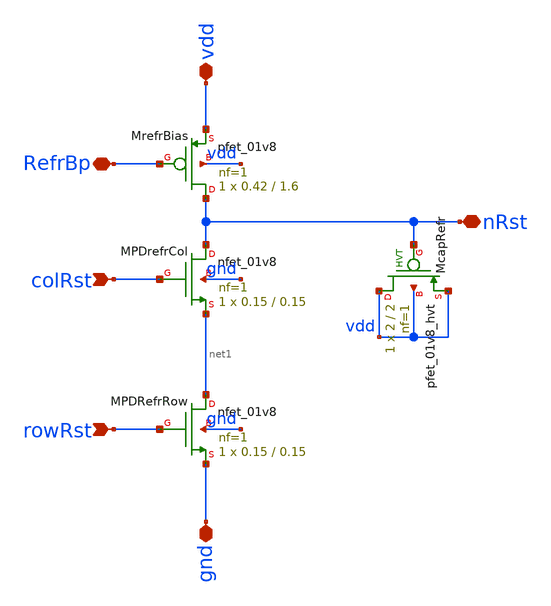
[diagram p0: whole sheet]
** sch_path: analog/xschem/PixelResetGen.sch
**.subckt PixelResetGen rowRst colRst RefrBp gnd vdd nRst
*.ipin rowRst
*.ipin colRst
*.iopin RefrBp
*.iopin gnd
*.iopin vdd
*.iopin nRst
XMPDrefrCol nRst colRst net1 gnd sky130_fd_pr__nfet_01v8 L=0.15 W=0.15 nf=1 ad='int((1 + 1)/2) * 0.15 / 1 * 0.29'
+ as='int((1 + 2)/2) * 0.15 / 1 * 0.29' pd='2*int((1 + 1)/2) * (0.15 / 1 + 0.29)' ps='2*int((1 + 2)/2) * (0.15 / 1 + 0.29)'
+ nrd='0.29 / 0.15 ' nrs='0.29 / 0.15 ' sa=0 sb=0 sd=0 mult=1 m=1
XMrefrBias nRst RefrBp vdd vdd sky130_fd_pr__pfet_01v8 L=1.6 W=0.42 nf=1 ad='int((1 + 1)/2) * 0.42 / 1 * 0.29'
+ as='int((1 + 2)/2) * 0.42 / 1 * 0.29' pd='2*int((1 + 1)/2) * (0.42 / 1 + 0.29)' ps='2*int((1 + 2)/2) * (0.42 / 1 + 0.29)'
+ nrd='0.29 / 0.42 ' nrs='0.29 / 0.42 ' sa=0 sb=0 sd=0 mult=1 m=1
XMcapRefr vdd nRst vdd vdd sky130_fd_pr__pfet_01v8_hvt L=2 W=2 nf=1 ad='int((1 + 1)/2) * 2 / 1 * 0.29'
+ as='int((1 + 2)/2) * 2 / 1 * 0.29' pd='2*int((1 + 1)/2) * (2 / 1 + 0.29)' ps='2*int((1 + 2)/2) * (2 / 1 + 0.29)'
+ nrd='0.29 / 2 ' nrs='0.29 / 2 ' sa=0 sb=0 sd=0 mult=1 m=1
XMPDRefrRow net1 rowRst gnd gnd sky130_fd_pr__nfet_01v8 L=0.15 W=0.15 nf=1 ad='int((1 + 1)/2) * 0.15 / 1 * 0.29'
+ as='int((1 + 2)/2) * 0.15 / 1 * 0.29' pd='2*int((1 + 1)/2) * (0.15 / 1 + 0.29)' ps='2*int((1 + 2)/2) * (0.15 / 1 + 0.29)'
+ nrd='0.29 / 0.15 ' nrs='0.29 / 0.15 ' sa=0 sb=0 sd=0 mult=1 m=1
**.ends
.end
